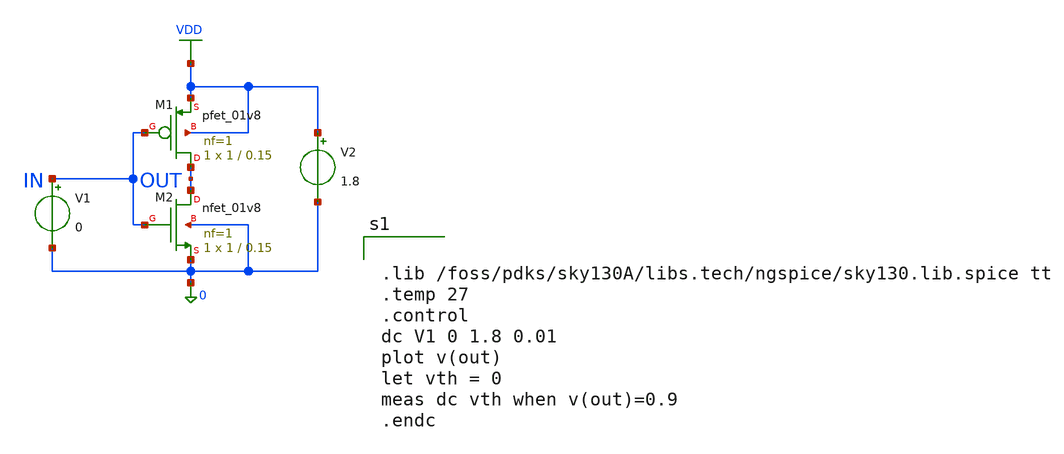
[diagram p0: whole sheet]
** sch_path: inverter.sch
**.subckt inverter
XM1 OUT IN VDD VDD sky130_fd_pr__pfet_01v8 L=0.15 W=1 nf=1 ad='int((1 + 1)/2) * 1 / 1 * 0.29' as='int((1 + 2)/2) * 1 / 1 * 0.29'
+ pd='2*int((1 + 1)/2) * (1 / 1 + 0.29)' ps='2*int((1 + 2)/2) * (1 / 1 + 0.29)' nrd='0.29 / 1 ' nrs='0.29 / 1 '
+ sa=0 sb=0 sd=0 mult=1 m=1
XM2 OUT IN 0 0 sky130_fd_pr__nfet_01v8 L=0.15 W=1 nf=1 ad='int((1 + 1)/2) * 1 / 1 * 0.29' as='int((1 + 2)/2) * 1 / 1 * 0.29'
+ pd='2*int((1 + 1)/2) * (1 / 1 + 0.29)' ps='2*int((1 + 2)/2) * (1 / 1 + 0.29)' nrd='0.29 / 1 ' nrs='0.29 / 1 '
+ sa=0 sb=0 sd=0 mult=1 m=1
V1 IN 0 0
V2 VDD 0 1.8
**** begin user architecture code


.lib /foss/pdks/sky130A/libs.tech/ngspice/sky130.lib.spice tt
.temp 27
.control
dc V1 0 1.8 0.01
plot v(out)
let vth = 0
meas dc vth when v(out)=0.9
.endc


**** end user architecture code
**.ends
.GLOBAL VDD
.end
